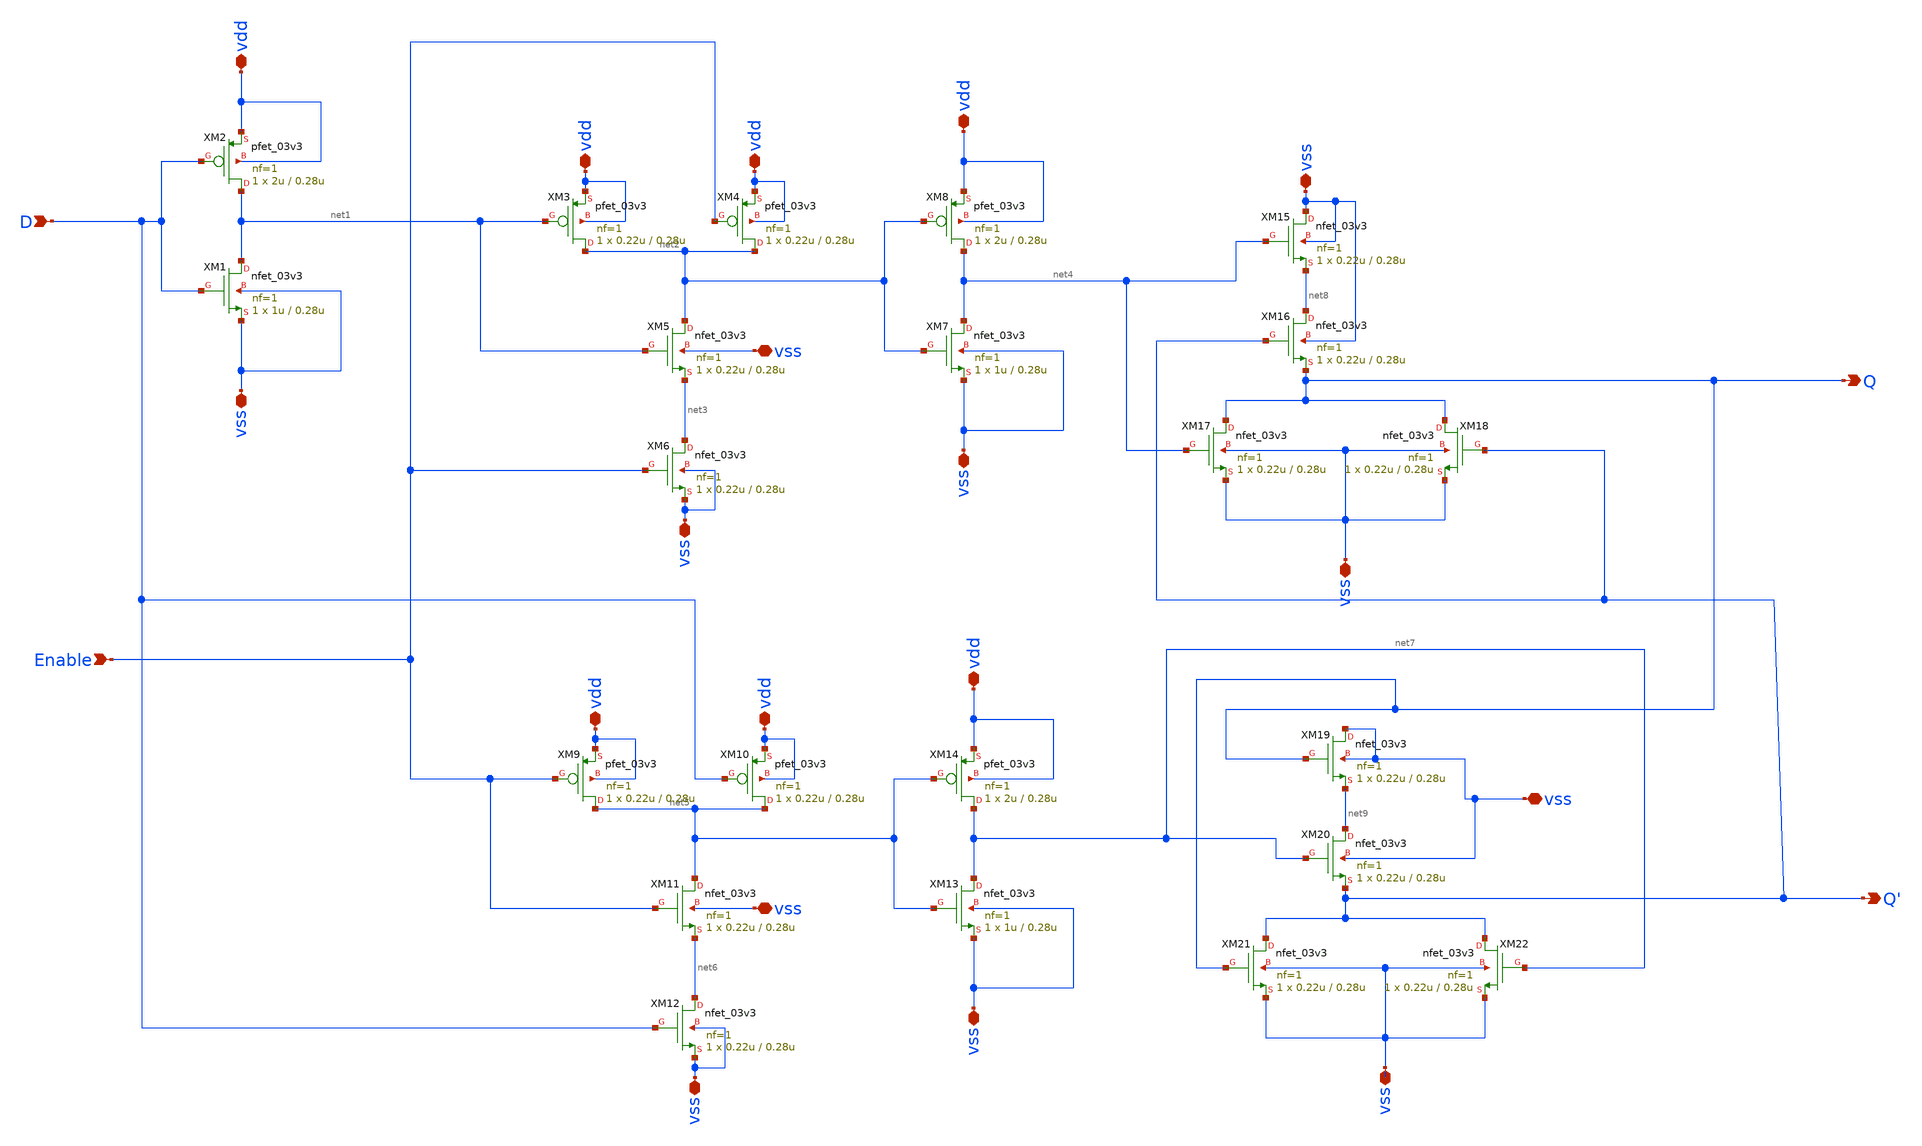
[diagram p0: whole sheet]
** sch_path: designs/DFFE/DFFE.sch
**.subckt DFFE vdd vss D vdd vdd vdd vss vdd vdd vdd vss Enable vss vss Q Q' vss vss vss vss vss vss
*.iopin vdd
*.iopin vss
*.ipin D
*.iopin vdd
*.iopin vdd
*.iopin vdd
*.iopin vss
*.iopin vdd
*.iopin vdd
*.iopin vdd
*.iopin vss
*.ipin Enable
*.iopin vss
*.iopin vss
*.opin Q
*.opin Q'
*.iopin vss
*.iopin vss
*.iopin vss
*.iopin vss
*.iopin vss
*.iopin vss
XM1 net1 D vss vss nfet_03v3 L=0.28u W=1u nf=1 ad='int((nf+1)/2) * W/nf * 0.18u' as='int((nf+2)/2) * W/nf * 0.18u'
+ pd='2*int((nf+1)/2) * (W/nf + 0.18u)' ps='2*int((nf+2)/2) * (W/nf + 0.18u)' nrd='0.18u / W' nrs='0.18u / W'
+ sa=0 sb=0 sd=0 m=1
XM2 net1 D vdd vdd pfet_03v3 L=0.28u W=2u nf=1 ad='int((nf+1)/2) * W/nf * 0.18u' as='int((nf+2)/2) * W/nf * 0.18u'
+ pd='2*int((nf+1)/2) * (W/nf + 0.18u)' ps='2*int((nf+2)/2) * (W/nf + 0.18u)' nrd='0.18u / W' nrs='0.18u / W'
+ sa=0 sb=0 sd=0 m=1
XM3 net2 net1 vdd vdd pfet_03v3 L=0.28u W=0.22u nf=1 ad='int((nf+1)/2) * W/nf * 0.18u' as='int((nf+2)/2) * W/nf * 0.18u'
+ pd='2*int((nf+1)/2) * (W/nf + 0.18u)' ps='2*int((nf+2)/2) * (W/nf + 0.18u)' nrd='0.18u / W' nrs='0.18u / W'
+ sa=0 sb=0 sd=0 m=1
XM4 net2 Enable vdd vdd pfet_03v3 L=0.28u W=0.22u nf=1 ad='int((nf+1)/2) * W/nf * 0.18u' as='int((nf+2)/2) * W/nf * 0.18u'
+ pd='2*int((nf+1)/2) * (W/nf + 0.18u)' ps='2*int((nf+2)/2) * (W/nf + 0.18u)' nrd='0.18u / W' nrs='0.18u / W'
+ sa=0 sb=0 sd=0 m=1
XM5 net2 net1 net3 vss nfet_03v3 L=0.28u W=0.22u nf=1 ad='int((nf+1)/2) * W/nf * 0.18u' as='int((nf+2)/2) * W/nf * 0.18u'
+ pd='2*int((nf+1)/2) * (W/nf + 0.18u)' ps='2*int((nf+2)/2) * (W/nf + 0.18u)' nrd='0.18u / W' nrs='0.18u / W'
+ sa=0 sb=0 sd=0 m=1
XM6 net3 Enable vss vss nfet_03v3 L=0.28u W=0.22u nf=1 ad='int((nf+1)/2) * W/nf * 0.18u' as='int((nf+2)/2) * W/nf * 0.18u'
+ pd='2*int((nf+1)/2) * (W/nf + 0.18u)' ps='2*int((nf+2)/2) * (W/nf + 0.18u)' nrd='0.18u / W' nrs='0.18u / W'
+ sa=0 sb=0 sd=0 m=1
XM7 net4 net2 vss vss nfet_03v3 L=0.28u W=1u nf=1 ad='int((nf+1)/2) * W/nf * 0.18u' as='int((nf+2)/2) * W/nf * 0.18u'
+ pd='2*int((nf+1)/2) * (W/nf + 0.18u)' ps='2*int((nf+2)/2) * (W/nf + 0.18u)' nrd='0.18u / W' nrs='0.18u / W'
+ sa=0 sb=0 sd=0 m=1
XM8 net4 net2 vdd vdd pfet_03v3 L=0.28u W=2u nf=1 ad='int((nf+1)/2) * W/nf * 0.18u' as='int((nf+2)/2) * W/nf * 0.18u'
+ pd='2*int((nf+1)/2) * (W/nf + 0.18u)' ps='2*int((nf+2)/2) * (W/nf + 0.18u)' nrd='0.18u / W' nrs='0.18u / W'
+ sa=0 sb=0 sd=0 m=1
XM9 net5 Enable vdd vdd pfet_03v3 L=0.28u W=0.22u nf=1 ad='int((nf+1)/2) * W/nf * 0.18u' as='int((nf+2)/2) * W/nf * 0.18u'
+ pd='2*int((nf+1)/2) * (W/nf + 0.18u)' ps='2*int((nf+2)/2) * (W/nf + 0.18u)' nrd='0.18u / W' nrs='0.18u / W'
+ sa=0 sb=0 sd=0 m=1
XM10 net5 D vdd vdd pfet_03v3 L=0.28u W=0.22u nf=1 ad='int((nf+1)/2) * W/nf * 0.18u' as='int((nf+2)/2) * W/nf * 0.18u'
+ pd='2*int((nf+1)/2) * (W/nf + 0.18u)' ps='2*int((nf+2)/2) * (W/nf + 0.18u)' nrd='0.18u / W' nrs='0.18u / W'
+ sa=0 sb=0 sd=0 m=1
XM11 net5 Enable net6 vss nfet_03v3 L=0.28u W=0.22u nf=1 ad='int((nf+1)/2) * W/nf * 0.18u' as='int((nf+2)/2) * W/nf * 0.18u'
+ pd='2*int((nf+1)/2) * (W/nf + 0.18u)' ps='2*int((nf+2)/2) * (W/nf + 0.18u)' nrd='0.18u / W' nrs='0.18u / W'
+ sa=0 sb=0 sd=0 m=1
XM12 net6 D vss vss nfet_03v3 L=0.28u W=0.22u nf=1 ad='int((nf+1)/2) * W/nf * 0.18u' as='int((nf+2)/2) * W/nf * 0.18u'
+ pd='2*int((nf+1)/2) * (W/nf + 0.18u)' ps='2*int((nf+2)/2) * (W/nf + 0.18u)' nrd='0.18u / W' nrs='0.18u / W'
+ sa=0 sb=0 sd=0 m=1
XM13 net7 net5 vss vss nfet_03v3 L=0.28u W=1u nf=1 ad='int((nf+1)/2) * W/nf * 0.18u' as='int((nf+2)/2) * W/nf * 0.18u'
+ pd='2*int((nf+1)/2) * (W/nf + 0.18u)' ps='2*int((nf+2)/2) * (W/nf + 0.18u)' nrd='0.18u / W' nrs='0.18u / W'
+ sa=0 sb=0 sd=0 m=1
XM14 net7 net5 vdd vdd pfet_03v3 L=0.28u W=2u nf=1 ad='int((nf+1)/2) * W/nf * 0.18u' as='int((nf+2)/2) * W/nf * 0.18u'
+ pd='2*int((nf+1)/2) * (W/nf + 0.18u)' ps='2*int((nf+2)/2) * (W/nf + 0.18u)' nrd='0.18u / W' nrs='0.18u / W'
+ sa=0 sb=0 sd=0 m=1
XM15 vss net4 net8 vss nfet_03v3 L=0.28u W=0.22u nf=1 ad='int((nf+1)/2) * W/nf * 0.18u' as='int((nf+2)/2) * W/nf * 0.18u'
+ pd='2*int((nf+1)/2) * (W/nf + 0.18u)' ps='2*int((nf+2)/2) * (W/nf + 0.18u)' nrd='0.18u / W' nrs='0.18u / W'
+ sa=0 sb=0 sd=0 m=1
XM16 net8 Q' Q vss nfet_03v3 L=0.28u W=0.22u nf=1 ad='int((nf+1)/2) * W/nf * 0.18u' as='int((nf+2)/2)
+ * W/nf * 0.18u' pd='2*int((nf+1)/2) * (W/nf + 0.18u)' ps='2*int((nf+2)/2) * (W/nf + 0.18u)' nrd='0.18u
+ / W' nrs='0.18u / W' sa=0 sb=0 sd=0 m=1
XM17 Q net4 vss vss nfet_03v3 L=0.28u W=0.22u nf=1 ad='int((nf+1)/2) * W/nf * 0.18u' as='int((nf+2)/2)
+ * W/nf * 0.18u' pd='2*int((nf+1)/2) * (W/nf + 0.18u)' ps='2*int((nf+2)/2) * (W/nf + 0.18u)' nrd='0.18u
+ / W' nrs='0.18u / W' sa=0 sb=0 sd=0 m=1
XM18 Q Q' vss vss nfet_03v3 L=0.28u W=0.22u nf=1 ad='int((nf+1)/2) * W/nf * 0.18u' as='int((nf+2)/2) * W/nf * 0.18u'
+ pd='2*int((nf+1)/2) * (W/nf + 0.18u)' ps='2*int((nf+2)/2) * (W/nf + 0.18u)' nrd='0.18u / W' nrs='0.18u / W'
+ sa=0 sb=0 sd=0 m=1
XM19 vss Q net9 vss nfet_03v3 L=0.28u W=0.22u nf=1 ad='int((nf+1)/2) * W/nf * 0.18u' as='int((nf+2)/2) * W/nf * 0.18u'
+ pd='2*int((nf+1)/2) * (W/nf + 0.18u)' ps='2*int((nf+2)/2) * (W/nf + 0.18u)' nrd='0.18u / W' nrs='0.18u / W'
+ sa=0 sb=0 sd=0 m=1
XM20 net9 net7 Q' vss nfet_03v3 L=0.28u W=0.22u nf=1 ad='int((nf+1)/2) * W/nf * 0.18u' as='int((nf+2)/2)
+ * W/nf * 0.18u' pd='2*int((nf+1)/2) * (W/nf + 0.18u)' ps='2*int((nf+2)/2) * (W/nf + 0.18u)' nrd='0.18u
+ / W' nrs='0.18u / W' sa=0 sb=0 sd=0 m=1
XM21 Q' Q vss vss nfet_03v3 L=0.28u W=0.22u nf=1 ad='int((nf+1)/2) * W/nf * 0.18u' as='int((nf+2)/2) * W/nf * 0.18u'
+ pd='2*int((nf+1)/2) * (W/nf + 0.18u)' ps='2*int((nf+2)/2) * (W/nf + 0.18u)' nrd='0.18u / W' nrs='0.18u / W'
+ sa=0 sb=0 sd=0 m=1
XM22 Q' net7 vss vss nfet_03v3 L=0.28u W=0.22u nf=1 ad='int((nf+1)/2) * W/nf * 0.18u' as='int((nf+2)/2)
+ * W/nf * 0.18u' pd='2*int((nf+1)/2) * (W/nf + 0.18u)' ps='2*int((nf+2)/2) * (W/nf + 0.18u)' nrd='0.18u
+ / W' nrs='0.18u / W' sa=0 sb=0 sd=0 m=1
**.ends
.end
